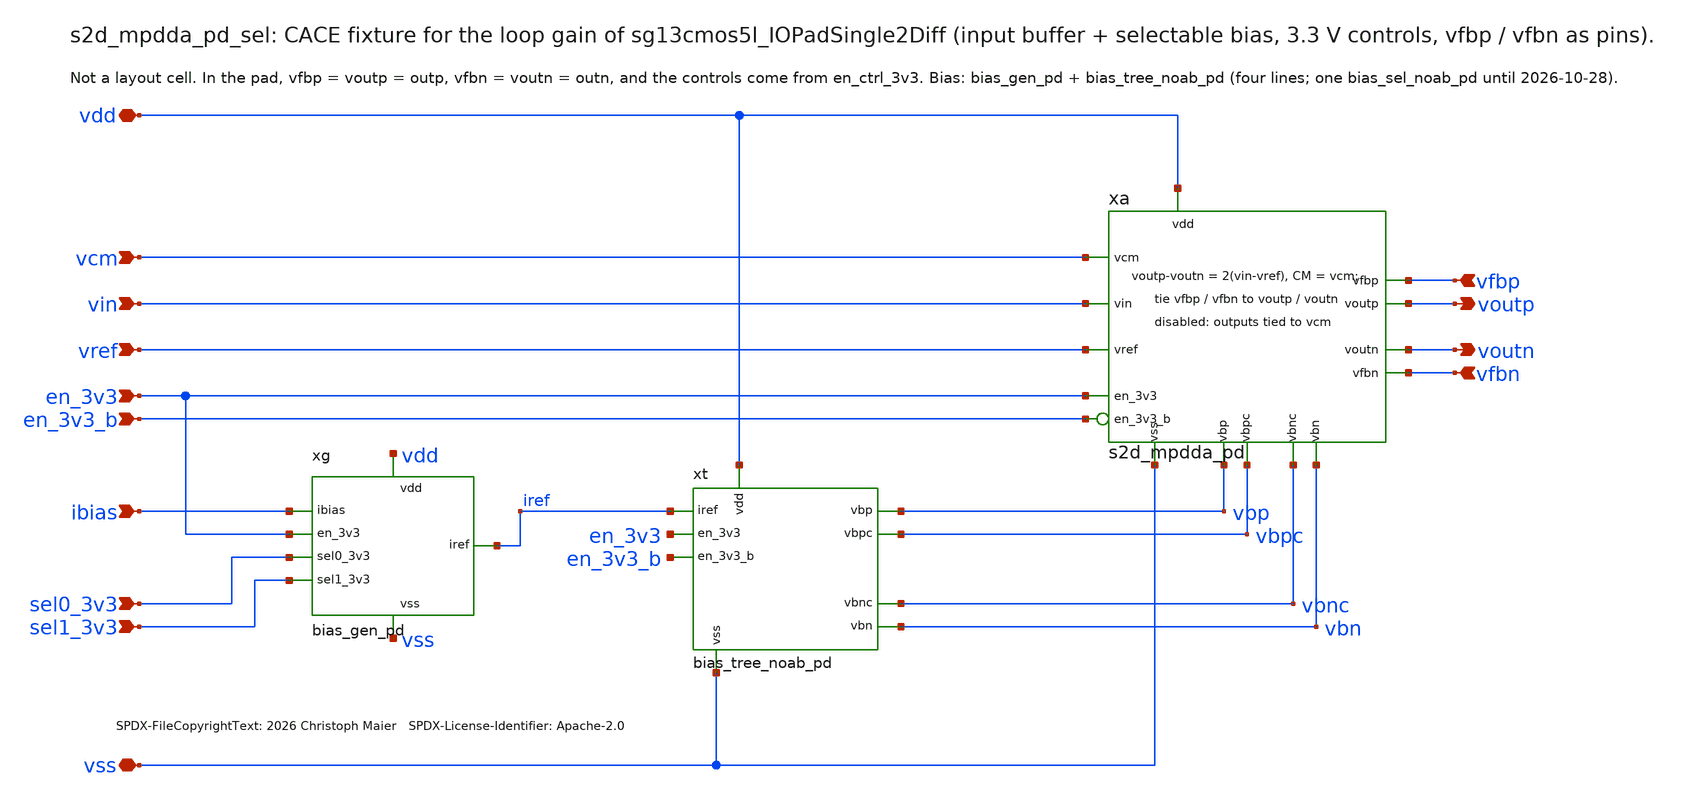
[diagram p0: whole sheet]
** sch_path: macros/sg13cmos5l_IOPadSingle2Diff/schematic/xschem/s2d_mpdda_pd_sel.sch
* SPDX-FileCopyrightText: 2026 Christoph Maier SPDX-License-Identifier: Apache-2.0
**.subckt s2d_mpdda_pd_sel vdd vin vref vcm en_3v3 en_3v3_b ibias sel0_3v3 sel1_3v3 vss voutp voutn
*+ vfbp vfbn
*.iopin vdd
*.ipin vin
*.ipin vref
*.ipin vcm
*.ipin en_3v3
*.ipin en_3v3_b
*.ipin ibias
*.ipin sel0_3v3
*.ipin sel1_3v3
*.iopin vss
*.opin voutp
*.opin voutn
*.ipin vfbp
*.ipin vfbn
xa vdd vss vin vref vcm voutp voutn vfbp vfbn vbp vbn vbpc vbnc en_3v3 en_3v3_b s2d_mpdda_pd
xg vdd vss ibias iref en_3v3 sel0_3v3 sel1_3v3 bias_gen_pd
xt vdd vss iref vbp vbn vbpc vbnc en_3v3 en_3v3_b bias_tree_noab_pd
**.ends
.end
